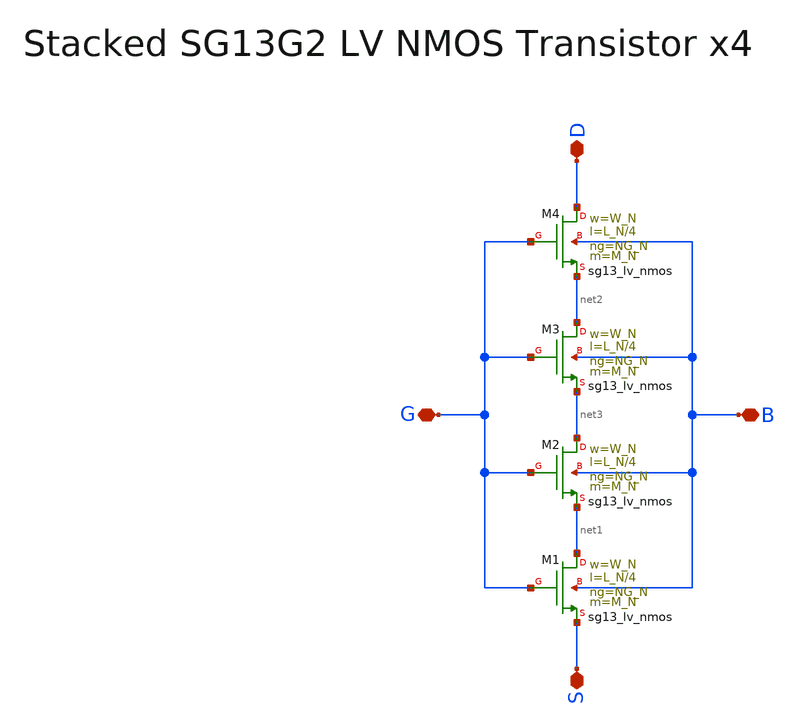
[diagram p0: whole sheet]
** sch_path: SG13G2_ATBS-ADC-main/xschem/stacked_transistors/sg13g2_lv_nmos_stacked/sg13g2_lv_nmos_stacked_x4.sch
**.subckt sg13g2_lv_nmos_stacked_x4 D S G B
*.iopin D
*.iopin S
*.iopin G
*.iopin B
XM1 net1 G S B sg13_lv_nmos w=W_N l=L_N/4 ng=NG_N m=M_N mm_ok=1
XM2 net3 G net1 B sg13_lv_nmos w=W_N l=L_N/4 ng=NG_N m=M_N mm_ok=1
XM3 net2 G net3 B sg13_lv_nmos w=W_N l=L_N/4 ng=NG_N m=M_N mm_ok=1
XM4 D G net2 B sg13_lv_nmos w=W_N l=L_N/4 ng=NG_N m=M_N mm_ok=1
**.ends
.end
